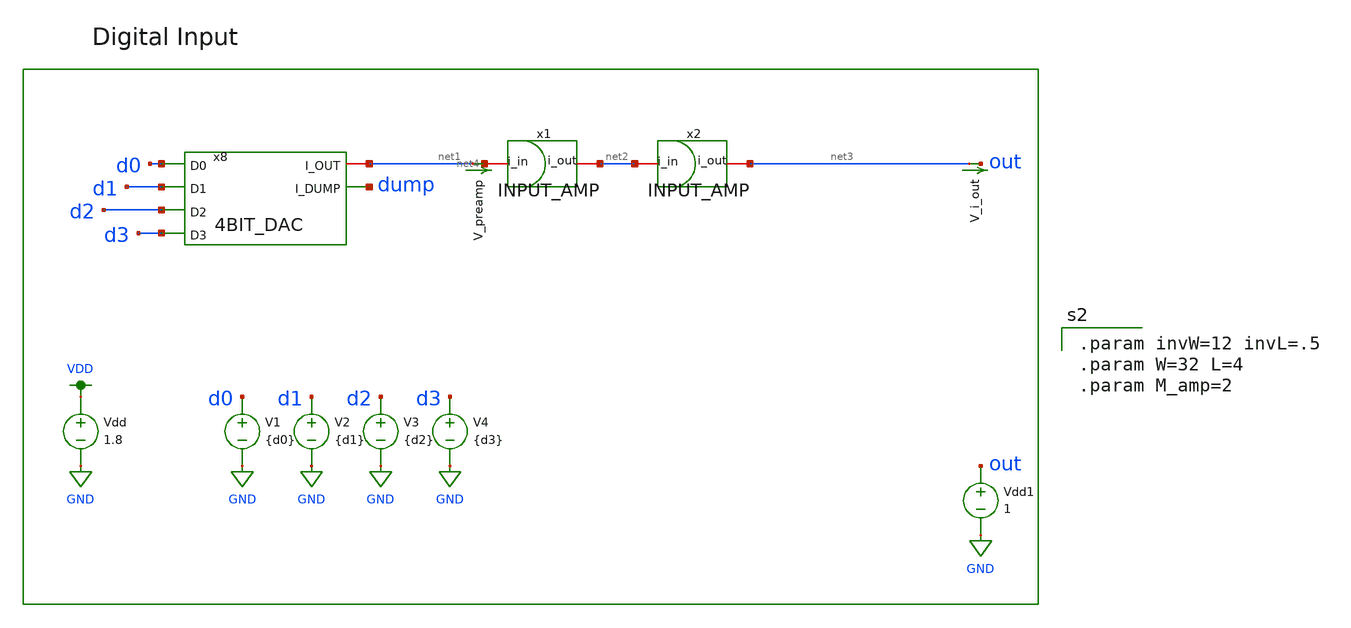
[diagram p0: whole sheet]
** sch_path: schemas/dac_testbench.sch
**.subckt dac_testbench
x8 net1 dump d1 d0 d2 d3 4BIT_DAC
V_i_out net3 out 0
.save i(v_i_out)
V2 d1 GND {d1}
V1 d0 GND {d0}
V3 d2 GND {d2}
V4 d3 GND {d3}
Vdd VDD GND 1.8
Vdd1 out GND 1
x1 net4 net2 INPUT_AMP
V_preamp net1 net4 0
.save i(v_preamp)
x2 net2 net3 INPUT_AMP
**** begin user architecture code


.param state=0
.param d0=1.8*state
.param d1=1.8*state
.param d2=1.8*state
.param d3=1.8*state
.tran .01n 30n

.control
  run
  .save all
  plot i(v_i_out)  i(v_preamp)

.endc



.option wnflag=1
.lib ~/skywater/skywater-pdk/libraries/sky130_fd_pr_ngspice/latest/models/sky130.lib.spice tt


.param invW=12 invL=.5
.param W=32 L=4
.param M_amp=2


**** end user architecture code
**.ends

* expanding   symbol:  /home/lxbtlr/DTILO/schemas/4BIT_DAC.sym # of pins=6
** sym_path: schemas/4BIT_DAC.sym
** sch_path: schemas/4BIT_DAC.sch
.subckt 4BIT_DAC I_OUT I_DUMP D1 D0 D2 D3
*.ipin D3
*.ipin D2
*.ipin D1
*.ipin D0
*.opin I_DUMP
*.iopin I_OUT
XM13 net1 GND net2 GND sky130_fd_pr__nfet_01v8 L={L} W={W} nf=1 ad='int((nf+1)/2) * W/nf * 0.29' as='int((nf+2)/2) * W/nf * 0.29'
+ pd='2*int((nf+1)/2) * (W/nf + 0.29)' ps='2*int((nf+2)/2) * (W/nf + 0.29)' nrd='0.29 / W' nrs='0.29 / W'
+ sa=0 sb=0 sd=0 mult=1 m=1
XM14 net2 D3 net14 GND sky130_fd_pr__nfet_01v8 L={L} W={W} nf=1 ad='int((nf+1)/2) * W/nf * 0.29' as='int((nf+2)/2) * W/nf * 0.29'
+ pd='2*int((nf+1)/2) * (W/nf + 0.29)' ps='2*int((nf+2)/2) * (W/nf + 0.29)' nrd='0.29 / W' nrs='0.29 / W'
+ sa=0 sb=0 sd=0 mult=1 m=1
XM15 net1 GND net4 GND sky130_fd_pr__nfet_01v8 L={L} W={W} nf=1 ad='int((nf+1)/2) * W/nf * 0.29' as='int((nf+2)/2) * W/nf * 0.29'
+ pd='2*int((nf+1)/2) * (W/nf + 0.29)' ps='2*int((nf+2)/2) * (W/nf + 0.29)' nrd='0.29 / W' nrs='0.29 / W'
+ sa=0 sb=0 sd=0 mult=1 m=1
XM16 net2 net3 I_DUMP GND sky130_fd_pr__nfet_01v8 L={L} W={W} nf=1 ad='int((nf+1)/2) * W/nf * 0.29' as='int((nf+2)/2) * W/nf * 0.29'
+ pd='2*int((nf+1)/2) * (W/nf + 0.29)' ps='2*int((nf+2)/2) * (W/nf + 0.29)' nrd='0.29 / W' nrs='0.29 / W'
+ sa=0 sb=0 sd=0 mult=1 m=1
XM17 net4 GND net5 GND sky130_fd_pr__nfet_01v8 L={L} W={W} nf=1 ad='int((nf+1)/2) * W/nf * 0.29' as='int((nf+2)/2) * W/nf * 0.29'
+ pd='2*int((nf+1)/2) * (W/nf + 0.29)' ps='2*int((nf+2)/2) * (W/nf + 0.29)' nrd='0.29 / W' nrs='0.29 / W'
+ sa=0 sb=0 sd=0 mult=1 m=1
XM18 net5 D2 net14 GND sky130_fd_pr__nfet_01v8 L={L} W={W} nf=1 ad='int((nf+1)/2) * W/nf * 0.29' as='int((nf+2)/2) * W/nf * 0.29'
+ pd='2*int((nf+1)/2) * (W/nf + 0.29)' ps='2*int((nf+2)/2) * (W/nf + 0.29)' nrd='0.29 / W' nrs='0.29 / W'
+ sa=0 sb=0 sd=0 mult=1 m=1
XM19 net4 GND net7 GND sky130_fd_pr__nfet_01v8 L={L} W={W} nf=1 ad='int((nf+1)/2) * W/nf * 0.29' as='int((nf+2)/2) * W/nf * 0.29'
+ pd='2*int((nf+1)/2) * (W/nf + 0.29)' ps='2*int((nf+2)/2) * (W/nf + 0.29)' nrd='0.29 / W' nrs='0.29 / W'
+ sa=0 sb=0 sd=0 mult=1 m=1
XM20 net5 net6 I_DUMP GND sky130_fd_pr__nfet_01v8 L={L} W={W} nf=1 ad='int((nf+1)/2) * W/nf * 0.29' as='int((nf+2)/2) * W/nf * 0.29'
+ pd='2*int((nf+1)/2) * (W/nf + 0.29)' ps='2*int((nf+2)/2) * (W/nf + 0.29)' nrd='0.29 / W' nrs='0.29 / W'
+ sa=0 sb=0 sd=0 mult=1 m=1
XM21 net7 GND net8 GND sky130_fd_pr__nfet_01v8 L={L} W={W} nf=1 ad='int((nf+1)/2) * W/nf * 0.29' as='int((nf+2)/2) * W/nf * 0.29'
+ pd='2*int((nf+1)/2) * (W/nf + 0.29)' ps='2*int((nf+2)/2) * (W/nf + 0.29)' nrd='0.29 / W' nrs='0.29 / W'
+ sa=0 sb=0 sd=0 mult=1 m=1
XM22 net8 D1 net14 GND sky130_fd_pr__nfet_01v8 L={L} W={W} nf=1 ad='int((nf+1)/2) * W/nf * 0.29' as='int((nf+2)/2) * W/nf * 0.29'
+ pd='2*int((nf+1)/2) * (W/nf + 0.29)' ps='2*int((nf+2)/2) * (W/nf + 0.29)' nrd='0.29 / W' nrs='0.29 / W'
+ sa=0 sb=0 sd=0 mult=1 m=1
XM23 net7 GND net10 GND sky130_fd_pr__nfet_01v8 L={L} W={W} nf=1 ad='int((nf+1)/2) * W/nf * 0.29' as='int((nf+2)/2) * W/nf * 0.29'
+ pd='2*int((nf+1)/2) * (W/nf + 0.29)' ps='2*int((nf+2)/2) * (W/nf + 0.29)' nrd='0.29 / W' nrs='0.29 / W'
+ sa=0 sb=0 sd=0 mult=1 m=1
XM24 net8 net9 I_DUMP GND sky130_fd_pr__nfet_01v8 L={L} W={W} nf=1 ad='int((nf+1)/2) * W/nf * 0.29' as='int((nf+2)/2) * W/nf * 0.29'
+ pd='2*int((nf+1)/2) * (W/nf + 0.29)' ps='2*int((nf+2)/2) * (W/nf + 0.29)' nrd='0.29 / W' nrs='0.29 / W'
+ sa=0 sb=0 sd=0 mult=1 m=1
XM25 net10 GND net11 GND sky130_fd_pr__nfet_01v8 L={L} W={W} nf=1 ad='int((nf+1)/2) * W/nf * 0.29' as='int((nf+2)/2) * W/nf * 0.29'
+ pd='2*int((nf+1)/2) * (W/nf + 0.29)' ps='2*int((nf+2)/2) * (W/nf + 0.29)' nrd='0.29 / W' nrs='0.29 / W'
+ sa=0 sb=0 sd=0 mult=1 m=1
XM26 net11 D0 net14 GND sky130_fd_pr__nfet_01v8 L={L} W={W} nf=1 ad='int((nf+1)/2) * W/nf * 0.29' as='int((nf+2)/2) * W/nf * 0.29'
+ pd='2*int((nf+1)/2) * (W/nf + 0.29)' ps='2*int((nf+2)/2) * (W/nf + 0.29)' nrd='0.29 / W' nrs='0.29 / W'
+ sa=0 sb=0 sd=0 mult=1 m=1
XM27 net10 GND net13 GND sky130_fd_pr__nfet_01v8 L={L} W={W} nf=1 ad='int((nf+1)/2) * W/nf * 0.29' as='int((nf+2)/2) * W/nf * 0.29'
+ pd='2*int((nf+1)/2) * (W/nf + 0.29)' ps='2*int((nf+2)/2) * (W/nf + 0.29)' nrd='0.29 / W' nrs='0.29 / W'
+ sa=0 sb=0 sd=0 mult=1 m=1
XM28 net11 net12 I_DUMP GND sky130_fd_pr__nfet_01v8 L={L} W={W} nf=1 ad='int((nf+1)/2) * W/nf * 0.29'
+ as='int((nf+2)/2) * W/nf * 0.29' pd='2*int((nf+1)/2) * (W/nf + 0.29)' ps='2*int((nf+2)/2) * (W/nf + 0.29)'
+ nrd='0.29 / W' nrs='0.29 / W' sa=0 sb=0 sd=0 mult=1 m=1
XM29 net13 GND I_DUMP GND sky130_fd_pr__nfet_01v8 L={L} W={W} nf=1 ad='int((nf+1)/2) * W/nf * 0.29' as='int((nf+2)/2) * W/nf * 0.29'
+ pd='2*int((nf+1)/2) * (W/nf + 0.29)' ps='2*int((nf+2)/2) * (W/nf + 0.29)' nrd='0.29 / W' nrs='0.29 / W'
+ sa=0 sb=0 sd=0 mult=1 m=1
XM30 net16 VBP VDD VDD sky130_fd_pr__pfet_01v8 L={L} W={W} nf=1 ad='int((nf+1)/2) * W/nf * 0.29' as='int((nf+2)/2) * W/nf * 0.29'
+ pd='2*int((nf+1)/2) * (W/nf + 0.29)' ps='2*int((nf+2)/2) * (W/nf + 0.29)' nrd='0.29 / W' nrs='0.29 / W'
+ sa=0 sb=0 sd=0 mult=1 m=1
XM31 net16 net16 net17 GND sky130_fd_pr__nfet_01v8 L={L} W={W} nf=1 ad='int((nf+1)/2) * W/nf * 0.29'
+ as='int((nf+2)/2) * W/nf * 0.29' pd='2*int((nf+1)/2) * (W/nf + 0.29)' ps='2*int((nf+2)/2) * (W/nf + 0.29)'
+ nrd='0.29 / W' nrs='0.29 / W' sa=0 sb=0 sd=0 mult=8 m=8
XM32 net15 net15 VDD VDD sky130_fd_pr__pfet_01v8 L={L} W={W} nf=1 ad='int((nf+1)/2) * W/nf * 0.29' as='int((nf+2)/2) * W/nf * 0.29'
+ pd='2*int((nf+1)/2) * (W/nf + 0.29)' ps='2*int((nf+2)/2) * (W/nf + 0.29)' nrd='0.29 / W' nrs='0.29 / W'
+ sa=0 sb=0 sd=0 mult=1 m=1
XM33 VBP net15 VDD VDD sky130_fd_pr__pfet_01v8 L={L} W={W} nf=1 ad='int((nf+1)/2) * W/nf * 0.29' as='int((nf+2)/2) * W/nf * 0.29'
+ pd='2*int((nf+1)/2) * (W/nf + 0.29)' ps='2*int((nf+2)/2) * (W/nf + 0.29)' nrd='0.29 / W' nrs='0.29 / W'
+ sa=0 sb=0 sd=0 mult=1 m=1
XM34 VBN VBP VDD VDD sky130_fd_pr__pfet_01v8 L={L} W={W} nf=1 ad='int((nf+1)/2) * W/nf * 0.29' as='int((nf+2)/2) * W/nf * 0.29'
+ pd='2*int((nf+1)/2) * (W/nf + 0.29)' ps='2*int((nf+2)/2) * (W/nf + 0.29)' nrd='0.29 / W' nrs='0.29 / W'
+ sa=0 sb=0 sd=0 mult=1 m=1
XM35 VBP VBN GND GND sky130_fd_pr__nfet_01v8 L={L} W={W} nf=1 ad='int((nf+1)/2) * W/nf * 0.29' as='int((nf+2)/2) * W/nf * 0.29'
+ pd='2*int((nf+1)/2) * (W/nf + 0.29)' ps='2*int((nf+2)/2) * (W/nf + 0.29)' nrd='0.29 / W' nrs='0.29 / W'
+ sa=0 sb=0 sd=0 mult=1 m=1
XM36 VBN VBN GND GND sky130_fd_pr__nfet_01v8 L={L} W={W} nf=1 ad='int((nf+1)/2) * W/nf * 0.29' as='int((nf+2)/2) * W/nf * 0.29'
+ pd='2*int((nf+1)/2) * (W/nf + 0.29)' ps='2*int((nf+2)/2) * (W/nf + 0.29)' nrd='0.29 / W' nrs='0.29 / W'
+ sa=0 sb=0 sd=0 mult=1 m=1
XM37 net15 net16 GND GND sky130_fd_pr__nfet_01v8 L={L} W={W} nf=1 ad='int((nf+1)/2) * W/nf * 0.29' as='int((nf+2)/2) * W/nf * 0.29'
+ pd='2*int((nf+1)/2) * (W/nf + 0.29)' ps='2*int((nf+2)/2) * (W/nf + 0.29)' nrd='0.29 / W' nrs='0.29 / W'
+ sa=0 sb=0 sd=0 mult=1 m=1
R1 net17 GND {R} m=1
XM48 net18 VBP VDD VDD sky130_fd_pr__pfet_01v8 L={L} W={W} nf=1 ad='int((nf+1)/2) * W/nf * 0.29' as='int((nf+2)/2) * W/nf * 0.29'
+ pd='2*int((nf+1)/2) * (W/nf + 0.29)' ps='2*int((nf+2)/2) * (W/nf + 0.29)' nrd='0.29 / W' nrs='0.29 / W'
+ sa=0 sb=0 sd=0 mult=1 m=1
XM49 net20 VBP net18 VDD sky130_fd_pr__pfet_01v8 L={L} W={W} nf=1 ad='int((nf+1)/2) * W/nf * 0.29' as='int((nf+2)/2) * W/nf * 0.29'
+ pd='2*int((nf+1)/2) * (W/nf + 0.29)' ps='2*int((nf+2)/2) * (W/nf + 0.29)' nrd='0.29 / W' nrs='0.29 / W'
+ sa=0 sb=0 sd=0 mult=1 m=1
XM50 net20 net20 net23 GND sky130_fd_pr__nfet_01v8 L={L} W={W} nf=1 ad='int((nf+1)/2) * W/nf * 0.29'
+ as='int((nf+2)/2) * W/nf * 0.29' pd='2*int((nf+1)/2) * (W/nf + 0.29)' ps='2*int((nf+2)/2) * (W/nf + 0.29)'
+ nrd='0.29 / W' nrs='0.29 / W' sa=0 sb=0 sd=0 mult=4 m=4
XM51 net19 VBP VDD VDD sky130_fd_pr__pfet_01v8 L={L} W={W} nf=1 ad='int((nf+1)/2) * W/nf * 0.29' as='int((nf+2)/2) * W/nf * 0.29'
+ pd='2*int((nf+1)/2) * (W/nf + 0.29)' ps='2*int((nf+2)/2) * (W/nf + 0.29)' nrd='0.29 / W' nrs='0.29 / W'
+ sa=0 sb=0 sd=0 mult=1 m=1
XM52 net21 VBP net19 VDD sky130_fd_pr__pfet_01v8 L={L} W={W} nf=1 ad='int((nf+1)/2) * W/nf * 0.29' as='int((nf+2)/2) * W/nf * 0.29'
+ pd='2*int((nf+1)/2) * (W/nf + 0.29)' ps='2*int((nf+2)/2) * (W/nf + 0.29)' nrd='0.29 / W' nrs='0.29 / W'
+ sa=0 sb=0 sd=0 mult=1 m=1
XM53 net21 net21 net24 GND sky130_fd_pr__nfet_01v8 L={L} W={W} nf=1 ad='int((nf+1)/2) * W/nf * 0.29'
+ as='int((nf+2)/2) * W/nf * 0.29' pd='2*int((nf+1)/2) * (W/nf + 0.29)' ps='2*int((nf+2)/2) * (W/nf + 0.29)'
+ nrd='0.29 / W' nrs='0.29 / W' sa=0 sb=0 sd=0 mult=4 m=4
XM54 net22 net22 net23 GND sky130_fd_pr__nfet_01v8 L={L} W={W} nf=1 ad='int((nf+1)/2) * W/nf * 0.29'
+ as='int((nf+2)/2) * W/nf * 0.29' pd='2*int((nf+1)/2) * (W/nf + 0.29)' ps='2*int((nf+2)/2) * (W/nf + 0.29)'
+ nrd='0.29 / W' nrs='0.29 / W' sa=0 sb=0 sd=0 mult=1 m=1
XM55 I_OUT net22 net24 GND sky130_fd_pr__nfet_01v8 L={L} W={W} nf=1 ad='int((nf+1)/2) * W/nf * 0.29'
+ as='int((nf+2)/2) * W/nf * 0.29' pd='2*int((nf+1)/2) * (W/nf + 0.29)' ps='2*int((nf+2)/2) * (W/nf + 0.29)'
+ nrd='0.29 / W' nrs='0.29 / W' sa=0 sb=0 sd=0 mult=1 m=1
XM56 net24 net20 GND GND sky130_fd_pr__nfet_01v8 L={L} W={W} nf=1 ad='int((nf+1)/2) * W/nf * 0.29' as='int((nf+2)/2) * W/nf * 0.29'
+ pd='2*int((nf+1)/2) * (W/nf + 0.29)' ps='2*int((nf+2)/2) * (W/nf + 0.29)' nrd='0.29 / W' nrs='0.29 / W'
+ sa=0 sb=0 sd=0 mult=1 m=1
XM57 net23 net20 GND GND sky130_fd_pr__nfet_01v8 L={L} W={W} nf=1 ad='int((nf+1)/2) * W/nf * 0.29' as='int((nf+2)/2) * W/nf * 0.29'
+ pd='2*int((nf+1)/2) * (W/nf + 0.29)' ps='2*int((nf+2)/2) * (W/nf + 0.29)' nrd='0.29 / W' nrs='0.29 / W'
+ sa=0 sb=0 sd=0 mult=1 m=1
XM58 net25 VBP VDD VDD sky130_fd_pr__pfet_01v8 L={L} W={W} nf=1 ad='int((nf+1)/2) * W/nf * 0.29' as='int((nf+2)/2) * W/nf * 0.29'
+ pd='2*int((nf+1)/2) * (W/nf + 0.29)' ps='2*int((nf+2)/2) * (W/nf + 0.29)' nrd='0.29 / W' nrs='0.29 / W'
+ sa=0 sb=0 sd=0 mult=1/5 m=1/5
XM59 VCN VBP VDD VDD sky130_fd_pr__pfet_01v8 L={L} W={W} nf=1 ad='int((nf+1)/2) * W/nf * 0.29' as='int((nf+2)/2) * W/nf * 0.29'
+ pd='2*int((nf+1)/2) * (W/nf + 0.29)' ps='2*int((nf+2)/2) * (W/nf + 0.29)' nrd='0.29 / W' nrs='0.29 / W'
+ sa=0 sb=0 sd=0 mult=1 m=1
XM60 net25 net25 net26 GND sky130_fd_pr__nfet_01v8 L={L} W={W} nf=1 ad='int((nf+1)/2) * W/nf * 0.29'
+ as='int((nf+2)/2) * W/nf * 0.29' pd='2*int((nf+1)/2) * (W/nf + 0.29)' ps='2*int((nf+2)/2) * (W/nf + 0.29)'
+ nrd='0.29 / W' nrs='0.29 / W' sa=0 sb=0 sd=0 mult=4 m=4
XM61 net26 net25 GND GND sky130_fd_pr__nfet_01v8 L={L} W={W} nf=1 ad='int((nf+1)/2) * W/nf * 0.29' as='int((nf+2)/2) * W/nf * 0.29'
+ pd='2*int((nf+1)/2) * (W/nf + 0.29)' ps='2*int((nf+2)/2) * (W/nf + 0.29)' nrd='0.29 / W' nrs='0.29 / W'
+ sa=0 sb=0 sd=0 mult=1 m=1
XM62 net26 VCN VCN GND sky130_fd_pr__nfet_01v8 L={L} W={W} nf=1 ad='int((nf+1)/2) * W/nf * 0.29' as='int((nf+2)/2) * W/nf * 0.29'
+ pd='2*int((nf+1)/2) * (W/nf + 0.29)' ps='2*int((nf+2)/2) * (W/nf + 0.29)' nrd='0.29 / W' nrs='0.29 / W'
+ sa=0 sb=0 sd=0 mult=1 m=1
XM63 net27 VBP VDD VDD sky130_fd_pr__pfet_01v8 L={L} W={W} nf=1 ad='int((nf+1)/2) * W/nf * 0.29' as='int((nf+2)/2) * W/nf * 0.29'
+ pd='2*int((nf+1)/2) * (W/nf + 0.29)' ps='2*int((nf+2)/2) * (W/nf + 0.29)' nrd='0.29 / W' nrs='0.29 / W'
+ sa=0 sb=0 sd=0 mult=1 m=1
XM64 net31 VBP net27 VDD sky130_fd_pr__pfet_01v8 L={L} W={W} nf=1 ad='int((nf+1)/2) * W/nf * 0.29' as='int((nf+2)/2) * W/nf * 0.29'
+ pd='2*int((nf+1)/2) * (W/nf + 0.29)' ps='2*int((nf+2)/2) * (W/nf + 0.29)' nrd='0.29 / W' nrs='0.29 / W'
+ sa=0 sb=0 sd=0 mult=1 m=1
XM65 net28 VBP VDD VDD sky130_fd_pr__pfet_01v8 L={L} W={W} nf=1 ad='int((nf+1)/2) * W/nf * 0.29' as='int((nf+2)/2) * W/nf * 0.29'
+ pd='2*int((nf+1)/2) * (W/nf + 0.29)' ps='2*int((nf+2)/2) * (W/nf + 0.29)' nrd='0.29 / W' nrs='0.29 / W'
+ sa=0 sb=0 sd=0 mult=1 m=1
XM66 net32 VBP net28 VDD sky130_fd_pr__pfet_01v8 L={L} W={W} nf=1 ad='int((nf+1)/2) * W/nf * 0.29' as='int((nf+2)/2) * W/nf * 0.29'
+ pd='2*int((nf+1)/2) * (W/nf + 0.29)' ps='2*int((nf+2)/2) * (W/nf + 0.29)' nrd='0.29 / W' nrs='0.29 / W'
+ sa=0 sb=0 sd=0 mult=1 m=1
XM67 net29 VBP VDD VDD sky130_fd_pr__pfet_01v8 L={L} W={W} nf=1 ad='int((nf+1)/2) * W/nf * 0.29' as='int((nf+2)/2) * W/nf * 0.29'
+ pd='2*int((nf+1)/2) * (W/nf + 0.29)' ps='2*int((nf+2)/2) * (W/nf + 0.29)' nrd='0.29 / W' nrs='0.29 / W'
+ sa=0 sb=0 sd=0 mult=1 m=1
XM68 net22 VBP net29 VDD sky130_fd_pr__pfet_01v8 L={L} W={W} nf=1 ad='int((nf+1)/2) * W/nf * 0.29' as='int((nf+2)/2) * W/nf * 0.29'
+ pd='2*int((nf+1)/2) * (W/nf + 0.29)' ps='2*int((nf+2)/2) * (W/nf + 0.29)' nrd='0.29 / W' nrs='0.29 / W'
+ sa=0 sb=0 sd=0 mult=1 m=1
XM69 I_DUMP VCN net31 GND sky130_fd_pr__nfet_01v8 L={L} W={W} nf=1 ad='int((nf+1)/2) * W/nf * 0.29' as='int((nf+2)/2) * W/nf * 0.29'
+ pd='2*int((nf+1)/2) * (W/nf + 0.29)' ps='2*int((nf+2)/2) * (W/nf + 0.29)' nrd='0.29 / W' nrs='0.29 / W'
+ sa=0 sb=0 sd=0 mult=1 m=1
XM70 GND net31 I_DUMP GND sky130_fd_pr__nfet_01v8 L={L} W={W} nf=1 ad='int((nf+1)/2) * W/nf * 0.29' as='int((nf+2)/2) * W/nf * 0.29'
+ pd='2*int((nf+1)/2) * (W/nf + 0.29)' ps='2*int((nf+2)/2) * (W/nf + 0.29)' nrd='0.29 / W' nrs='0.29 / W'
+ sa=0 sb=0 sd=0 mult=1 m=1
XM71 net14 VCN net32 GND sky130_fd_pr__nfet_01v8 L={L} W={W} nf=1 ad='int((nf+1)/2) * W/nf * 0.29' as='int((nf+2)/2) * W/nf * 0.29'
+ pd='2*int((nf+1)/2) * (W/nf + 0.29)' ps='2*int((nf+2)/2) * (W/nf + 0.29)' nrd='0.29 / W' nrs='0.29 / W'
+ sa=0 sb=0 sd=0 mult=1 m=1
XM72 GND net32 net14 GND sky130_fd_pr__nfet_01v8 L={L} W={W} nf=1 ad='int((nf+1)/2) * W/nf * 0.29' as='int((nf+2)/2) * W/nf * 0.29'
+ pd='2*int((nf+1)/2) * (W/nf + 0.29)' ps='2*int((nf+2)/2) * (W/nf + 0.29)' nrd='0.29 / W' nrs='0.29 / W'
+ sa=0 sb=0 sd=0 mult=1 m=1
XM73 net30 VCN net22 GND sky130_fd_pr__nfet_01v8 L={L} W={W} nf=1 ad='int((nf+1)/2) * W/nf * 0.29' as='int((nf+2)/2) * W/nf * 0.29'
+ pd='2*int((nf+1)/2) * (W/nf + 0.29)' ps='2*int((nf+2)/2) * (W/nf + 0.29)' nrd='0.29 / W' nrs='0.29 / W'
+ sa=0 sb=0 sd=0 mult=1 m=1
XM74 GND net32 net30 GND sky130_fd_pr__nfet_01v8 L={L} W={W} nf=1 ad='int((nf+1)/2) * W/nf * 0.29' as='int((nf+2)/2) * W/nf * 0.29'
+ pd='2*int((nf+1)/2) * (W/nf + 0.29)' ps='2*int((nf+2)/2) * (W/nf + 0.29)' nrd='0.29 / W' nrs='0.29 / W'
+ sa=0 sb=0 sd=0 mult=1 m=1
x1 net3 D3 inv
x2 net6 D2 inv
x3 net9 D1 inv
x4 net12 D0 inv
.ends


* expanding   symbol:  /home/lxbtlr/DTILO/schemas/INPUT_AMP.sym # of pins=2
** sym_path: schemas/INPUT_AMP.sym
** sch_path: schemas/INPUT_AMP.sch
.subckt INPUT_AMP i_in i_out
*.iopin i_out
*.iopin i_in
x1 net1 i_in gain_mirror
x2 i_out net1 PMOS_gain_mirror
.ends


* expanding   symbol:  /home/mstopyra/Documents/DTILO/inv.sym # of pins=2
** sym_path: schemas/inv.sym
** sch_path: schemas/inv.sch
.subckt inv Q A
*.ipin A
*.opin Q
XM1 Q A GND GND sky130_fd_pr__nfet_01v8 L=0.15 W=1 nf=1 ad='int((nf+1)/2) * W/nf * 0.29' as='int((nf+2)/2) * W/nf * 0.29'
+ pd='2*int((nf+1)/2) * (W/nf + 0.29)' ps='2*int((nf+2)/2) * (W/nf + 0.29)' nrd='0.29 / W' nrs='0.29 / W'
+ sa=0 sb=0 sd=0 mult=1 m=1
XM2 Q A VDD VDD sky130_fd_pr__pfet_01v8 L=0.15 W=1 nf=1 ad='int((nf+1)/2) * W/nf * 0.29' as='int((nf+2)/2) * W/nf * 0.29'
+ pd='2*int((nf+1)/2) * (W/nf + 0.29)' ps='2*int((nf+2)/2) * (W/nf + 0.29)' nrd='0.29 / W' nrs='0.29 / W'
+ sa=0 sb=0 sd=0 mult=1 m=1
.ends


* expanding   symbol:  /home/lxbtlr/DTILO/schemas/gain_mirror.sym # of pins=2
** sym_path: schemas/gain_mirror.sym
** sch_path: schemas/gain_mirror.sch
.subckt gain_mirror out in
*.iopin in
*.iopin out
XM1 in in GND GND sky130_fd_pr__nfet_01v8 L={L} W={W} nf=1 ad='int((nf+1)/2) * W/nf * 0.29' as='int((nf+2)/2) * W/nf * 0.29'
+ pd='2*int((nf+1)/2) * (W/nf + 0.29)' ps='2*int((nf+2)/2) * (W/nf + 0.29)' nrd='0.29 / W' nrs='0.29 / W'
+ sa=0 sb=0 sd=0 mult=1 m=1
XM2 out in GND GND sky130_fd_pr__nfet_01v8 L={L} W={W} nf=1 ad='int((nf+1)/2) * W/nf * 0.29' as='int((nf+2)/2) * W/nf * 0.29'
+ pd='2*int((nf+1)/2) * (W/nf + 0.29)' ps='2*int((nf+2)/2) * (W/nf + 0.29)' nrd='0.29 / W' nrs='0.29 / W'
+ sa=0 sb=0 sd=0 mult={M_amp} m={M_amp}
XM3 out in GND GND sky130_fd_pr__nfet_01v8 L={L} W={W} nf=1 ad='int((nf+1)/2) * W/nf * 0.29' as='int((nf+2)/2) * W/nf * 0.29'
+ pd='2*int((nf+1)/2) * (W/nf + 0.29)' ps='2*int((nf+2)/2) * (W/nf + 0.29)' nrd='0.29 / W' nrs='0.29 / W'
+ sa=0 sb=0 sd=0 mult={M_amp} m={M_amp}
XM4 out in GND GND sky130_fd_pr__nfet_01v8 L={L} W={W} nf=1 ad='int((nf+1)/2) * W/nf * 0.29' as='int((nf+2)/2) * W/nf * 0.29'
+ pd='2*int((nf+1)/2) * (W/nf + 0.29)' ps='2*int((nf+2)/2) * (W/nf + 0.29)' nrd='0.29 / W' nrs='0.29 / W'
+ sa=0 sb=0 sd=0 mult={M_amp} m={M_amp}
XM5 out in GND GND sky130_fd_pr__nfet_01v8 L={L} W={W} nf=1 ad='int((nf+1)/2) * W/nf * 0.29' as='int((nf+2)/2) * W/nf * 0.29'
+ pd='2*int((nf+1)/2) * (W/nf + 0.29)' ps='2*int((nf+2)/2) * (W/nf + 0.29)' nrd='0.29 / W' nrs='0.29 / W'
+ sa=0 sb=0 sd=0 mult={M_amp} m={M_amp}
XM6 out in GND GND sky130_fd_pr__nfet_01v8 L={L} W={W} nf=1 ad='int((nf+1)/2) * W/nf * 0.29' as='int((nf+2)/2) * W/nf * 0.29'
+ pd='2*int((nf+1)/2) * (W/nf + 0.29)' ps='2*int((nf+2)/2) * (W/nf + 0.29)' nrd='0.29 / W' nrs='0.29 / W'
+ sa=0 sb=0 sd=0 mult={M_amp} m={M_amp}
.ends


* expanding   symbol:  /home/lxbtlr/DTILO/schemas/PMOS_gain_mirror.sym # of pins=2
** sym_path: schemas/PMOS_gain_mirror.sym
** sch_path: schemas/PMOS_gain_mirror.sch
.subckt PMOS_gain_mirror out in
*.iopin in
*.iopin out
XM1 in in VDD VDD sky130_fd_pr__pfet_01v8 L={L} W={W} nf=1 ad='int((nf+1)/2) * W/nf * 0.29' as='int((nf+2)/2) * W/nf * 0.29'
+ pd='2*int((nf+1)/2) * (W/nf + 0.29)' ps='2*int((nf+2)/2) * (W/nf + 0.29)' nrd='0.29 / W' nrs='0.29 / W'
+ sa=0 sb=0 sd=0 mult=1 m=1
XM2 out in VDD VDD sky130_fd_pr__pfet_01v8 L={L} W={W} nf=1 ad='int((nf+1)/2) * W/nf * 0.29' as='int((nf+2)/2) * W/nf * 0.29'
+ pd='2*int((nf+1)/2) * (W/nf + 0.29)' ps='2*int((nf+2)/2) * (W/nf + 0.29)' nrd='0.29 / W' nrs='0.29 / W'
+ sa=0 sb=0 sd=0 mult={M_amp} m={M_amp}
XM3 out in VDD VDD sky130_fd_pr__pfet_01v8 L={L} W={W} nf=1 ad='int((nf+1)/2) * W/nf * 0.29' as='int((nf+2)/2) * W/nf * 0.29'
+ pd='2*int((nf+1)/2) * (W/nf + 0.29)' ps='2*int((nf+2)/2) * (W/nf + 0.29)' nrd='0.29 / W' nrs='0.29 / W'
+ sa=0 sb=0 sd=0 mult={M_amp} m={M_amp}
XM4 out in VDD VDD sky130_fd_pr__pfet_01v8 L={L} W={W} nf=1 ad='int((nf+1)/2) * W/nf * 0.29' as='int((nf+2)/2) * W/nf * 0.29'
+ pd='2*int((nf+1)/2) * (W/nf + 0.29)' ps='2*int((nf+2)/2) * (W/nf + 0.29)' nrd='0.29 / W' nrs='0.29 / W'
+ sa=0 sb=0 sd=0 mult={M_amp} m={M_amp}
XM5 out in VDD VDD sky130_fd_pr__pfet_01v8 L={L} W={W} nf=1 ad='int((nf+1)/2) * W/nf * 0.29' as='int((nf+2)/2) * W/nf * 0.29'
+ pd='2*int((nf+1)/2) * (W/nf + 0.29)' ps='2*int((nf+2)/2) * (W/nf + 0.29)' nrd='0.29 / W' nrs='0.29 / W'
+ sa=0 sb=0 sd=0 mult={M_amp} m={M_amp}
XM6 out in VDD VDD sky130_fd_pr__pfet_01v8 L={L} W={W} nf=1 ad='int((nf+1)/2) * W/nf * 0.29' as='int((nf+2)/2) * W/nf * 0.29'
+ pd='2*int((nf+1)/2) * (W/nf + 0.29)' ps='2*int((nf+2)/2) * (W/nf + 0.29)' nrd='0.29 / W' nrs='0.29 / W'
+ sa=0 sb=0 sd=0 mult={M_amp} m={M_amp}
.ends

.GLOBAL GND
.GLOBAL VDD
.end
